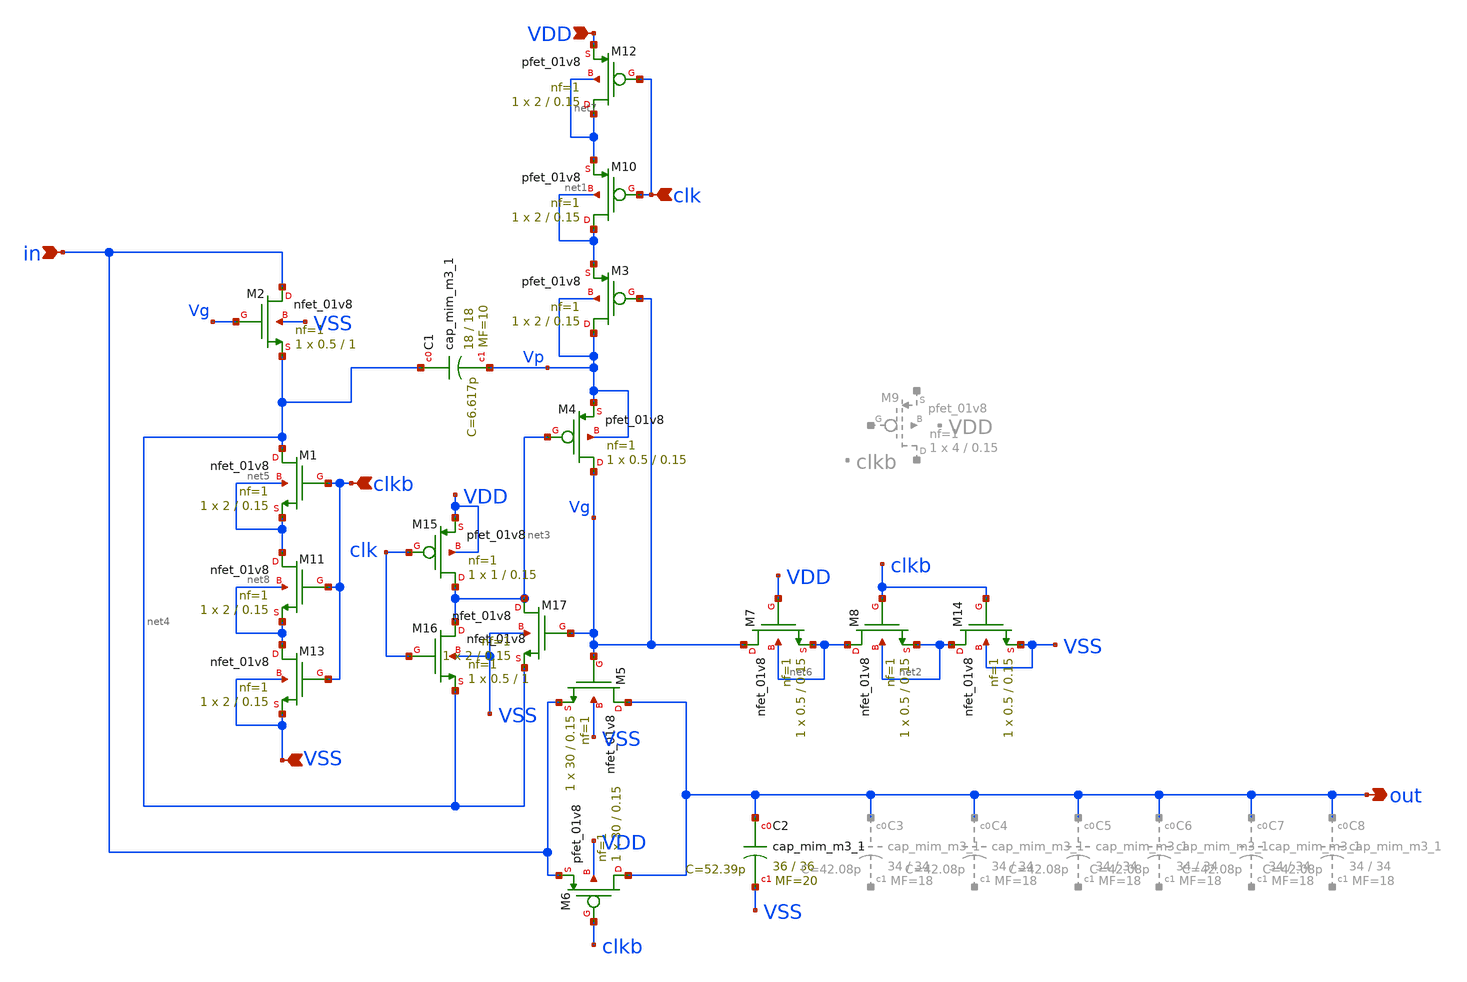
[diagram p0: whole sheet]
** sch_path: bootstrapped_switch.sch
**.subckt bootstrapped_switch in out VSS VDD clkb clk
*.ipin in
*.opin out
*.ipin VSS
*.ipin VDD
*.ipin clkb
*.ipin clk
XM1 net4 clkb net5 net5 sky130_fd_pr__nfet_01v8 L=0.15 W=2 nf=1 ad='int((nf+1)/2) * W/nf * 0.29' as='int((nf+2)/2) * W/nf * 0.29'
+ pd='2*int((nf+1)/2) * (W/nf + 0.29)' ps='2*int((nf+2)/2) * (W/nf + 0.29)' nrd='0.29 / W' nrs='0.29 / W'
+ sa=0 sb=0 sd=0 mult=1 m=1
XM2 in Vg net4 VSS sky130_fd_pr__nfet_01v8 L=1 W=0.5 nf=1 ad='int((nf+1)/2) * W/nf * 0.29' as='int((nf+2)/2) * W/nf * 0.29'
+ pd='2*int((nf+1)/2) * (W/nf + 0.29)' ps='2*int((nf+2)/2) * (W/nf + 0.29)' nrd='0.29 / W' nrs='0.29 / W'
+ sa=0 sb=0 sd=0 mult=1 m=1
XM3 Vp Vg net1 Vp sky130_fd_pr__pfet_01v8 L=0.15 W=2 nf=1 ad='int((nf+1)/2) * W/nf * 0.29' as='int((nf+2)/2) * W/nf * 0.29'
+ pd='2*int((nf+1)/2) * (W/nf + 0.29)' ps='2*int((nf+2)/2) * (W/nf + 0.29)' nrd='0.29 / W' nrs='0.29 / W'
+ sa=0 sb=0 sd=0 mult=1 m=1
XM5 out Vg in VSS sky130_fd_pr__nfet_01v8 L=0.15 W=30 nf=1 ad='int((nf+1)/2) * W/nf * 0.29' as='int((nf+2)/2) * W/nf * 0.29'
+ pd='2*int((nf+1)/2) * (W/nf + 0.29)' ps='2*int((nf+2)/2) * (W/nf + 0.29)' nrd='0.29 / W' nrs='0.29 / W'
+ sa=0 sb=0 sd=0 mult=1 m=1
XM6 out clkb in VDD sky130_fd_pr__pfet_01v8 L=0.15 W=30 nf=1 ad='int((nf+1)/2) * W/nf * 0.29' as='int((nf+2)/2) * W/nf * 0.29'
+ pd='2*int((nf+1)/2) * (W/nf + 0.29)' ps='2*int((nf+2)/2) * (W/nf + 0.29)' nrd='0.29 / W' nrs='0.29 / W'
+ sa=0 sb=0 sd=0 mult=1 m=1
XM8 net6 clkb net2 net2 sky130_fd_pr__nfet_01v8 L=0.15 W=0.5 nf=1 ad='int((nf+1)/2) * W/nf * 0.29' as='int((nf+2)/2) * W/nf * 0.29'
+ pd='2*int((nf+1)/2) * (W/nf + 0.29)' ps='2*int((nf+2)/2) * (W/nf + 0.29)' nrd='0.29 / W' nrs='0.29 / W'
+ sa=0 sb=0 sd=0 mult=1 m=1
XC1 net4 Vp sky130_fd_pr__cap_mim_m3_1 W=18 L=18 MF=10 m=10
XM7 Vg VDD net6 net6 sky130_fd_pr__nfet_01v8 L=0.15 W=0.5 nf=1 ad='int((nf+1)/2) * W/nf * 0.29' as='int((nf+2)/2) * W/nf * 0.29'
+ pd='2*int((nf+1)/2) * (W/nf + 0.29)' ps='2*int((nf+2)/2) * (W/nf + 0.29)' nrd='0.29 / W' nrs='0.29 / W'
+ sa=0 sb=0 sd=0 mult=1 m=1
XM4 Vg net3 Vp Vp sky130_fd_pr__pfet_01v8 L=0.15 W=0.5 nf=1 ad='int((nf+1)/2) * W/nf * 0.29' as='int((nf+2)/2) * W/nf * 0.29'
+ pd='2*int((nf+1)/2) * (W/nf + 0.29)' ps='2*int((nf+2)/2) * (W/nf + 0.29)' nrd='0.29 / W' nrs='0.29 / W'
+ sa=0 sb=0 sd=0 mult=1 m=1
XC2 out VSS sky130_fd_pr__cap_mim_m3_1 W=36 L=36 MF=20 m=20
XM10 net1 clk net7 net1 sky130_fd_pr__pfet_01v8 L=0.15 W=2 nf=1 ad='int((nf+1)/2) * W/nf * 0.29' as='int((nf+2)/2) * W/nf * 0.29'
+ pd='2*int((nf+1)/2) * (W/nf + 0.29)' ps='2*int((nf+2)/2) * (W/nf + 0.29)' nrd='0.29 / W' nrs='0.29 / W'
+ sa=0 sb=0 sd=0 mult=1 m=1
XM11 net5 clkb net8 net8 sky130_fd_pr__nfet_01v8 L=0.15 W=2 nf=1 ad='int((nf+1)/2) * W/nf * 0.29' as='int((nf+2)/2) * W/nf * 0.29'
+ pd='2*int((nf+1)/2) * (W/nf + 0.29)' ps='2*int((nf+2)/2) * (W/nf + 0.29)' nrd='0.29 / W' nrs='0.29 / W'
+ sa=0 sb=0 sd=0 mult=1 m=1
XM12 net7 clk VDD net7 sky130_fd_pr__pfet_01v8 L=0.15 W=2 nf=1 ad='int((nf+1)/2) * W/nf * 0.29' as='int((nf+2)/2) * W/nf * 0.29'
+ pd='2*int((nf+1)/2) * (W/nf + 0.29)' ps='2*int((nf+2)/2) * (W/nf + 0.29)' nrd='0.29 / W' nrs='0.29 / W'
+ sa=0 sb=0 sd=0 mult=1 m=1
XM13 net8 clkb VSS VSS sky130_fd_pr__nfet_01v8 L=0.15 W=2 nf=1 ad='int((nf+1)/2) * W/nf * 0.29' as='int((nf+2)/2) * W/nf * 0.29'
+ pd='2*int((nf+1)/2) * (W/nf + 0.29)' ps='2*int((nf+2)/2) * (W/nf + 0.29)' nrd='0.29 / W' nrs='0.29 / W'
+ sa=0 sb=0 sd=0 mult=1 m=1
XM14 net2 clkb VSS VSS sky130_fd_pr__nfet_01v8 L=0.15 W=0.5 nf=1 ad='int((nf+1)/2) * W/nf * 0.29' as='int((nf+2)/2) * W/nf * 0.29'
+ pd='2*int((nf+1)/2) * (W/nf + 0.29)' ps='2*int((nf+2)/2) * (W/nf + 0.29)' nrd='0.29 / W' nrs='0.29 / W'
+ sa=0 sb=0 sd=0 mult=1 m=1
XM15 net3 clk VDD VDD sky130_fd_pr__pfet_01v8 L=0.15 W=1 nf=1 ad='int((nf+1)/2) * W/nf * 0.29' as='int((nf+2)/2) * W/nf * 0.29'
+ pd='2*int((nf+1)/2) * (W/nf + 0.29)' ps='2*int((nf+2)/2) * (W/nf + 0.29)' nrd='0.29 / W' nrs='0.29 / W'
+ sa=0 sb=0 sd=0 mult=1 m=1
XM16 net3 clk net4 VSS sky130_fd_pr__nfet_01v8 L=1 W=0.5 nf=1 ad='int((nf+1)/2) * W/nf * 0.29' as='int((nf+2)/2) * W/nf * 0.29'
+ pd='2*int((nf+1)/2) * (W/nf + 0.29)' ps='2*int((nf+2)/2) * (W/nf + 0.29)' nrd='0.29 / W' nrs='0.29 / W'
+ sa=0 sb=0 sd=0 mult=1 m=1
XM17 net3 Vg net4 VSS sky130_fd_pr__nfet_01v8 L=0.15 W=2 nf=1 ad='int((nf+1)/2) * W/nf * 0.29' as='int((nf+2)/2) * W/nf * 0.29'
+ pd='2*int((nf+1)/2) * (W/nf + 0.29)' ps='2*int((nf+2)/2) * (W/nf + 0.29)' nrd='0.29 / W' nrs='0.29 / W'
+ sa=0 sb=0 sd=0 mult=1 m=1
**.ends
.end
